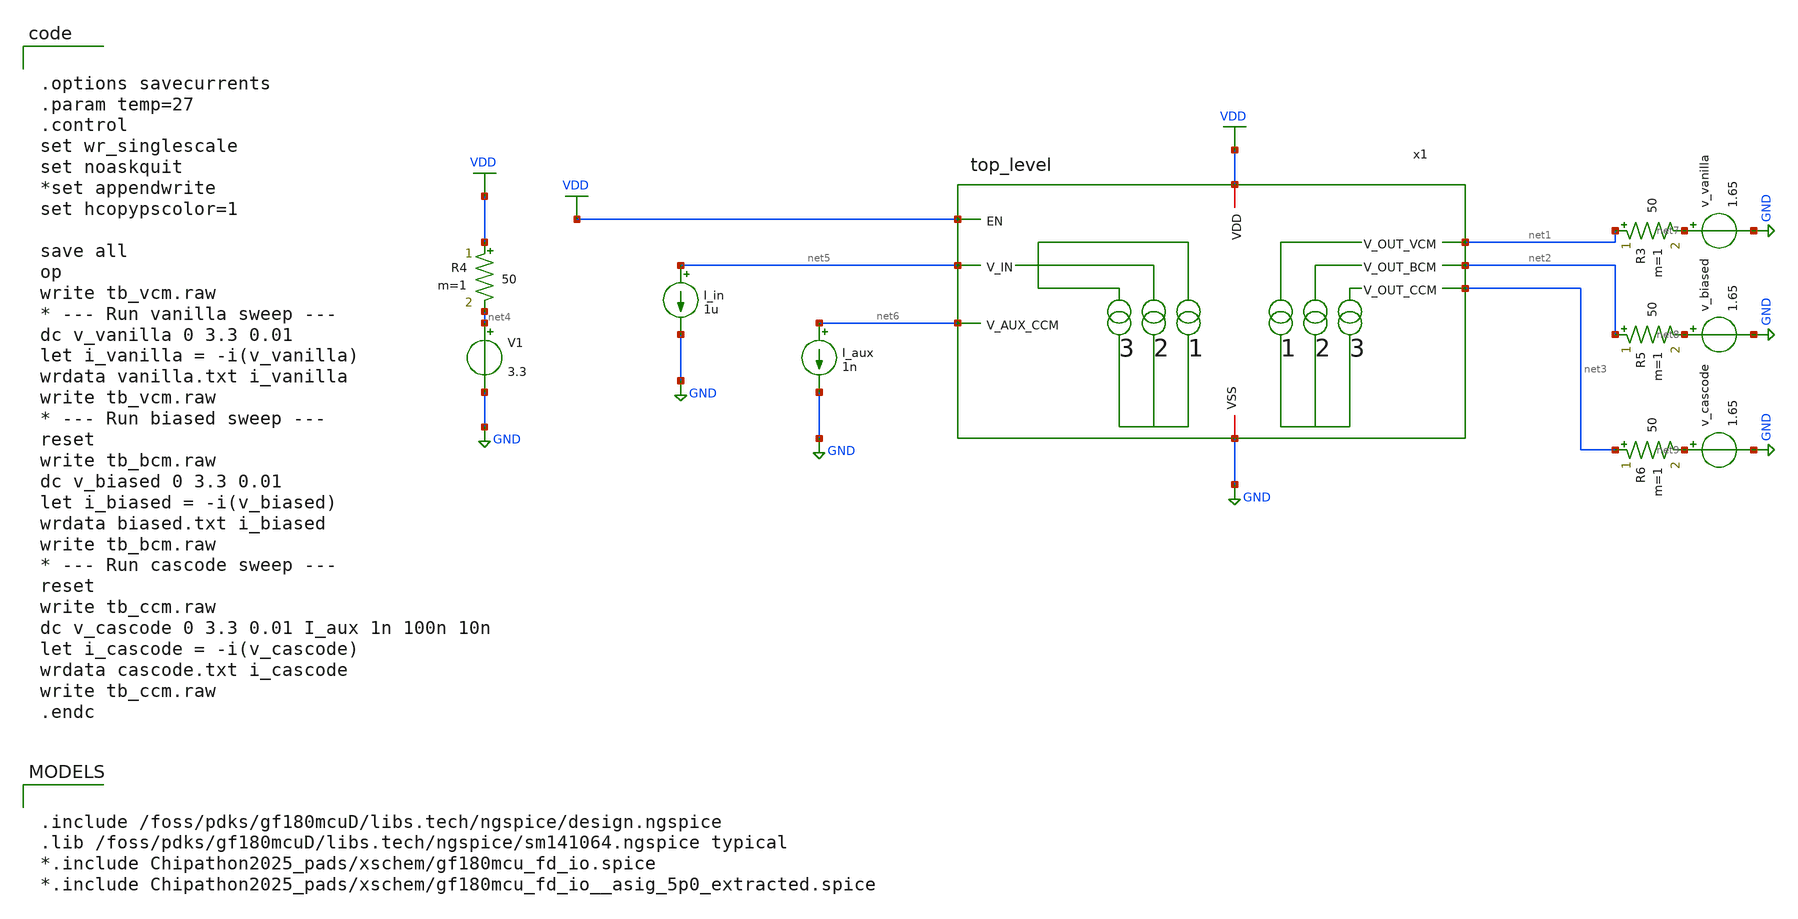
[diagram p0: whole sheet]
** sch_path: blocks/composite/regulated_cascoded_cmirror/xschem/testbench.sch
**.subckt testbench
V1 net4 GND 3.3
I_in net5 GND 1u
v_vanilla net7 GND 1.65
.save i(v_vanilla)
v_biased net8 GND 1.65
.save i(v_biased)
v_cascode net9 GND 1.65
.save i(v_cascode)
I_aux net6 GND 1n
R4 VDD net4 50 m=1
R3 net1 net7 50 m=1
R5 net2 net8 50 m=1
R6 net3 net9 50 m=1
x1 VDD VDD net5 net1 net2 net3 net6 GND top_level
**** begin user architecture code

.include /foss/pdks/gf180mcuD/libs.tech/ngspice/design.ngspice
.lib /foss/pdks/gf180mcuD/libs.tech/ngspice/sm141064.ngspice typical
*.include Chipathon2025_pads/xschem/gf180mcu_fd_io.spice
*.include Chipathon2025_pads/xschem/gf180mcu_fd_io__asig_5p0_extracted.spice



.options savecurrents
.param temp=27
.control
set wr_singlescale
set noaskquit
*set appendwrite
set hcopypscolor=1

save all
op
write tb_vcm.raw
* --- Run vanilla sweep ---
dc v_vanilla 0 3.3 0.01
let i_vanilla = -i(v_vanilla)
wrdata vanilla.txt i_vanilla
write tb_vcm.raw
* --- Run biased sweep ---
reset
write tb_bcm.raw
dc v_biased 0 3.3 0.01
let i_biased = -i(v_biased)
wrdata biased.txt i_biased
write tb_bcm.raw
* --- Run cascode sweep ---
reset
write tb_ccm.raw
dc v_cascode 0 3.3 0.01 I_aux 1n 100n 10n
let i_cascode = -i(v_cascode)
wrdata cascode.txt i_cascode
write tb_ccm.raw
.endc


**** end user architecture code
**.ends

* expanding   symbol:  top_level.sym # of pins=8
** sym_path: blocks/composite/regulated_cascoded_cmirror/xschem/top_level.sym
** sch_path: blocks/composite/regulated_cascoded_cmirror/xschem/top_level.sch
.subckt top_level VDD EN V_IN V_OUT_VCM V_OUT_BCM V_OUT_CCM V_AUX_CCM VSS
*.iopin VSS
*.ipin V_AUX_CCM
*.iopin VDD
*.opin V_OUT_VCM
*.opin V_OUT_BCM
*.opin V_OUT_CCM
*.ipin V_IN
*.ipin EN
XM1 net1 net1 VDD VDD pfet_03v3 L=2.0u W=40.0u nf=10 ad='int((nf+1)/2) * W/nf * 0.18u' as='int((nf+2)/2) * W/nf * 0.18u'
+ pd='2*int((nf+1)/2) * (W/nf + 0.18u)' ps='2*int((nf+2)/2) * (W/nf + 0.18u)' nrd='0.18u / W' nrs='0.18u / W'
+ sa=0 sb=0 sd=0 m=1
XM2 V_IN V_IN net1 VDD pfet_03v3 L=2.0u W=60.0u nf=15 ad='int((nf+1)/2) * W/nf * 0.18u' as='int((nf+2)/2) * W/nf * 0.18u'
+ pd='2*int((nf+1)/2) * (W/nf + 0.18u)' ps='2*int((nf+2)/2) * (W/nf + 0.18u)' nrd='0.18u / W' nrs='0.18u / W'
+ sa=0 sb=0 sd=0 m=1
XM3 net2 net1 VDD VDD pfet_03v3 L=2.0u W=40.0u nf=10 ad='int((nf+1)/2) * W/nf * 0.18u' as='int((nf+2)/2) * W/nf * 0.18u'
+ pd='2*int((nf+1)/2) * (W/nf + 0.18u)' ps='2*int((nf+2)/2) * (W/nf + 0.18u)' nrd='0.18u / W' nrs='0.18u / W'
+ sa=0 sb=0 sd=0 m=1
XM4 net3 V_IN net2 VDD pfet_03v3 L=2.0u W=60.0u nf=15 ad='int((nf+1)/2) * W/nf * 0.18u' as='int((nf+2)/2) * W/nf * 0.18u'
+ pd='2*int((nf+1)/2) * (W/nf + 0.18u)' ps='2*int((nf+2)/2) * (W/nf + 0.18u)' nrd='0.18u / W' nrs='0.18u / W'
+ sa=0 sb=0 sd=0 m=1
XM5 net7 net1 VDD VDD pfet_03v3 L=2.0u W=40.0u nf=10 ad='int((nf+1)/2) * W/nf * 0.18u' as='int((nf+2)/2) * W/nf * 0.18u'
+ pd='2*int((nf+1)/2) * (W/nf + 0.18u)' ps='2*int((nf+2)/2) * (W/nf + 0.18u)' nrd='0.18u / W' nrs='0.18u / W'
+ sa=0 sb=0 sd=0 m=1
XM6 net4 V_IN net7 VDD pfet_03v3 L=2.0u W=60.0u nf=15 ad='int((nf+1)/2) * W/nf * 0.18u' as='int((nf+2)/2) * W/nf * 0.18u'
+ pd='2*int((nf+1)/2) * (W/nf + 0.18u)' ps='2*int((nf+2)/2) * (W/nf + 0.18u)' nrd='0.18u / W' nrs='0.18u / W'
+ sa=0 sb=0 sd=0 m=1
XM7 net6 net1 VDD VDD pfet_03v3 L=2.0u W=40.0u nf=10 ad='int((nf+1)/2) * W/nf * 0.18u' as='int((nf+2)/2) * W/nf * 0.18u'
+ pd='2*int((nf+1)/2) * (W/nf + 0.18u)' ps='2*int((nf+2)/2) * (W/nf + 0.18u)' nrd='0.18u / W' nrs='0.18u / W'
+ sa=0 sb=0 sd=0 m=1
XM8 net5 V_IN net6 VDD pfet_03v3 L=2.0u W=60.0u nf=15 ad='int((nf+1)/2) * W/nf * 0.18u' as='int((nf+2)/2) * W/nf * 0.18u'
+ pd='2*int((nf+1)/2) * (W/nf + 0.18u)' ps='2*int((nf+2)/2) * (W/nf + 0.18u)' nrd='0.18u / W' nrs='0.18u / W'
+ sa=0 sb=0 sd=0 m=1
XM11 net8 net8 VDD VDD pfet_03v3 L=2.0u W=40.0u nf=10 ad='int((nf+1)/2) * W/nf * 0.18u' as='int((nf+2)/2) * W/nf * 0.18u'
+ pd='2*int((nf+1)/2) * (W/nf + 0.18u)' ps='2*int((nf+2)/2) * (W/nf + 0.18u)' nrd='0.18u / W' nrs='0.18u / W'
+ sa=0 sb=0 sd=0 m=1
XM12 V_AUX_CCM V_AUX_CCM net8 VDD pfet_03v3 L=2.0u W=60.0u nf=15 ad='int((nf+1)/2) * W/nf * 0.18u' as='int((nf+2)/2) * W/nf * 0.18u'
+ pd='2*int((nf+1)/2) * (W/nf + 0.18u)' ps='2*int((nf+2)/2) * (W/nf + 0.18u)' nrd='0.18u / W' nrs='0.18u / W'
+ sa=0 sb=0 sd=0 m=1
XM14 net1 EN VDD VDD pfet_03v3 L=2.0u W=40.0u nf=10 ad='int((nf+1)/2) * W/nf * 0.18u' as='int((nf+2)/2) * W/nf * 0.18u'
+ pd='2*int((nf+1)/2) * (W/nf + 0.18u)' ps='2*int((nf+2)/2) * (W/nf + 0.18u)' nrd='0.18u / W' nrs='0.18u / W'
+ sa=0 sb=0 sd=0 m=1
XM18 net1 EN VDD VDD pfet_03v3 L=2.0u W=40.0u nf=10 ad='int((nf+1)/2) * W/nf * 0.18u' as='int((nf+2)/2) * W/nf * 0.18u'
+ pd='2*int((nf+1)/2) * (W/nf + 0.18u)' ps='2*int((nf+2)/2) * (W/nf + 0.18u)' nrd='0.18u / W' nrs='0.18u / W'
+ sa=0 sb=0 sd=0 m=1
XM15 net1 EN VDD VDD pfet_03v3 L=2.0u W=40.0u nf=10 ad='int((nf+1)/2) * W/nf * 0.18u' as='int((nf+2)/2) * W/nf * 0.18u'
+ pd='2*int((nf+1)/2) * (W/nf + 0.18u)' ps='2*int((nf+2)/2) * (W/nf + 0.18u)' nrd='0.18u / W' nrs='0.18u / W'
+ sa=0 sb=0 sd=0 m=1
XM16 net8 EN VDD VDD pfet_03v3 L=2.0u W=40.0u nf=10 ad='int((nf+1)/2) * W/nf * 0.18u' as='int((nf+2)/2) * W/nf * 0.18u'
+ pd='2*int((nf+1)/2) * (W/nf + 0.18u)' ps='2*int((nf+2)/2) * (W/nf + 0.18u)' nrd='0.18u / W' nrs='0.18u / W'
+ sa=0 sb=0 sd=0 m=1
XM17 net10 net8 VDD VDD pfet_03v3 L=2.0u W=40.0u nf=10 ad='int((nf+1)/2) * W/nf * 0.18u' as='int((nf+2)/2) * W/nf * 0.18u'
+ pd='2*int((nf+1)/2) * (W/nf + 0.18u)' ps='2*int((nf+2)/2) * (W/nf + 0.18u)' nrd='0.18u / W' nrs='0.18u / W'
+ sa=0 sb=0 sd=0 m=1
XM19 net9 V_AUX_CCM net10 VDD pfet_03v3 L=2.0u W=60.0u nf=15 ad='int((nf+1)/2) * W/nf * 0.18u' as='int((nf+2)/2) * W/nf * 0.18u'
+ pd='2*int((nf+1)/2) * (W/nf + 0.18u)' ps='2*int((nf+2)/2) * (W/nf + 0.18u)' nrd='0.18u / W' nrs='0.18u / W'
+ sa=0 sb=0 sd=0 m=1
x1 net3 V_OUT_VCM VSS vanilla_cm
x2 V_OUT_BCM net4 VSS biased_cm
x3 V_OUT_CCM net9 net5 VSS cascode_cm
.ends


* expanding   symbol:  vanilla_cm.sym # of pins=3
** sym_path: vanilla_cm.sym
** sch_path: vanilla_cm.sch
.subckt vanilla_cm v_in v_out vss
*.ipin v_in
*.iopin vss
*.opin v_out
XM1 v_out v_in vss vss nfet_03v3 L=1u W=5u nf=1 ad='int((nf+1)/2) * W/nf * 0.18u' as='int((nf+2)/2) * W/nf * 0.18u'
+ pd='2*int((nf+1)/2) * (W/nf + 0.18u)' ps='2*int((nf+2)/2) * (W/nf + 0.18u)' nrd='0.18u / W' nrs='0.18u / W'
+ sa=0 sb=0 sd=0 m=1
XM2 v_in v_in vss vss nfet_03v3 L=1u W=5u nf=1 ad='int((nf+1)/2) * W/nf * 0.18u' as='int((nf+2)/2) * W/nf * 0.18u'
+ pd='2*int((nf+1)/2) * (W/nf + 0.18u)' ps='2*int((nf+2)/2) * (W/nf + 0.18u)' nrd='0.18u / W' nrs='0.18u / W'
+ sa=0 sb=0 sd=0 m=1
.ends


* expanding   symbol:  biased_cm.sym # of pins=3
** sym_path: biased_cm.sym
** sch_path: biased_cm.sch
.subckt biased_cm v_out v_in vss
*.ipin v_in
*.iopin vss
*.opin v_out
XM3 net2 net1 vss vss nfet_03v3 L=1u W=5u nf=1 ad='int((nf+1)/2) * W/nf * 0.18u' as='int((nf+2)/2) * W/nf * 0.18u'
+ pd='2*int((nf+1)/2) * (W/nf + 0.18u)' ps='2*int((nf+2)/2) * (W/nf + 0.18u)' nrd='0.18u / W' nrs='0.18u / W'
+ sa=0 sb=0 sd=0 m=1
XM4 net1 net1 vss vss nfet_03v3 L=1u W=5u nf=1 ad='int((nf+1)/2) * W/nf * 0.18u' as='int((nf+2)/2) * W/nf * 0.18u'
+ pd='2*int((nf+1)/2) * (W/nf + 0.18u)' ps='2*int((nf+2)/2) * (W/nf + 0.18u)' nrd='0.18u / W' nrs='0.18u / W'
+ sa=0 sb=0 sd=0 m=1
XM5 v_out v_in net2 vss nfet_03v3 L=1u W=5u nf=1 ad='int((nf+1)/2) * W/nf * 0.18u' as='int((nf+2)/2) * W/nf * 0.18u'
+ pd='2*int((nf+1)/2) * (W/nf + 0.18u)' ps='2*int((nf+2)/2) * (W/nf + 0.18u)' nrd='0.18u / W' nrs='0.18u / W'
+ sa=0 sb=0 sd=0 m=1
XM6 v_in v_in net1 vss nfet_03v3 L=1u W=5u nf=1 ad='int((nf+1)/2) * W/nf * 0.18u' as='int((nf+2)/2) * W/nf * 0.18u'
+ pd='2*int((nf+1)/2) * (W/nf + 0.18u)' ps='2*int((nf+2)/2) * (W/nf + 0.18u)' nrd='0.18u / W' nrs='0.18u / W'
+ sa=0 sb=0 sd=0 m=1
.ends


* expanding   symbol:  cascode_cm.sym # of pins=4
** sym_path: cascode_cm.sym
** sch_path: cascode_cm.sch
.subckt cascode_cm v_out v_aux v_in vss
*.ipin v_in
*.iopin vss
*.ipin v_aux
*.opin v_out
XM10 v_aux net1 vss vss nfet_03v3 L=1u W=5u nf=1 ad='int((nf+1)/2) * W/nf * 0.18u' as='int((nf+2)/2) * W/nf * 0.18u'
+ pd='2*int((nf+1)/2) * (W/nf + 0.18u)' ps='2*int((nf+2)/2) * (W/nf + 0.18u)' nrd='0.18u / W' nrs='0.18u / W'
+ sa=0 sb=0 sd=0 m=1
XM8 v_in v_aux net1 vss nfet_03v3 L=1u W=5u nf=1 ad='int((nf+1)/2) * W/nf * 0.18u' as='int((nf+2)/2) * W/nf * 0.18u'
+ pd='2*int((nf+1)/2) * (W/nf + 0.18u)' ps='2*int((nf+2)/2) * (W/nf + 0.18u)' nrd='0.18u / W' nrs='0.18u / W'
+ sa=0 sb=0 sd=0 m=1
XM11 net1 v_in vss vss nfet_03v3 L=1u W=5u nf=1 ad='int((nf+1)/2) * W/nf * 0.18u' as='int((nf+2)/2) * W/nf * 0.18u'
+ pd='2*int((nf+1)/2) * (W/nf + 0.18u)' ps='2*int((nf+2)/2) * (W/nf + 0.18u)' nrd='0.18u / W' nrs='0.18u / W'
+ sa=0 sb=0 sd=0 m=1
XM12 v_aux net2 vss vss nfet_03v3 L=1u W=5u nf=1 ad='int((nf+1)/2) * W/nf * 0.18u' as='int((nf+2)/2) * W/nf * 0.18u'
+ pd='2*int((nf+1)/2) * (W/nf + 0.18u)' ps='2*int((nf+2)/2) * (W/nf + 0.18u)' nrd='0.18u / W' nrs='0.18u / W'
+ sa=0 sb=0 sd=0 m=1
XM13 net2 v_in vss vss nfet_03v3 L=1u W=5u nf=1 ad='int((nf+1)/2) * W/nf * 0.18u' as='int((nf+2)/2) * W/nf * 0.18u'
+ pd='2*int((nf+1)/2) * (W/nf + 0.18u)' ps='2*int((nf+2)/2) * (W/nf + 0.18u)' nrd='0.18u / W' nrs='0.18u / W'
+ sa=0 sb=0 sd=0 m=1
XM14 v_out v_aux net2 vss nfet_03v3 L=1u W=5u nf=1 ad='int((nf+1)/2) * W/nf * 0.18u' as='int((nf+2)/2) * W/nf * 0.18u'
+ pd='2*int((nf+1)/2) * (W/nf + 0.18u)' ps='2*int((nf+2)/2) * (W/nf + 0.18u)' nrd='0.18u / W' nrs='0.18u / W'
+ sa=0 sb=0 sd=0 m=1
.ends

.GLOBAL GND
.GLOBAL VDD
.end
